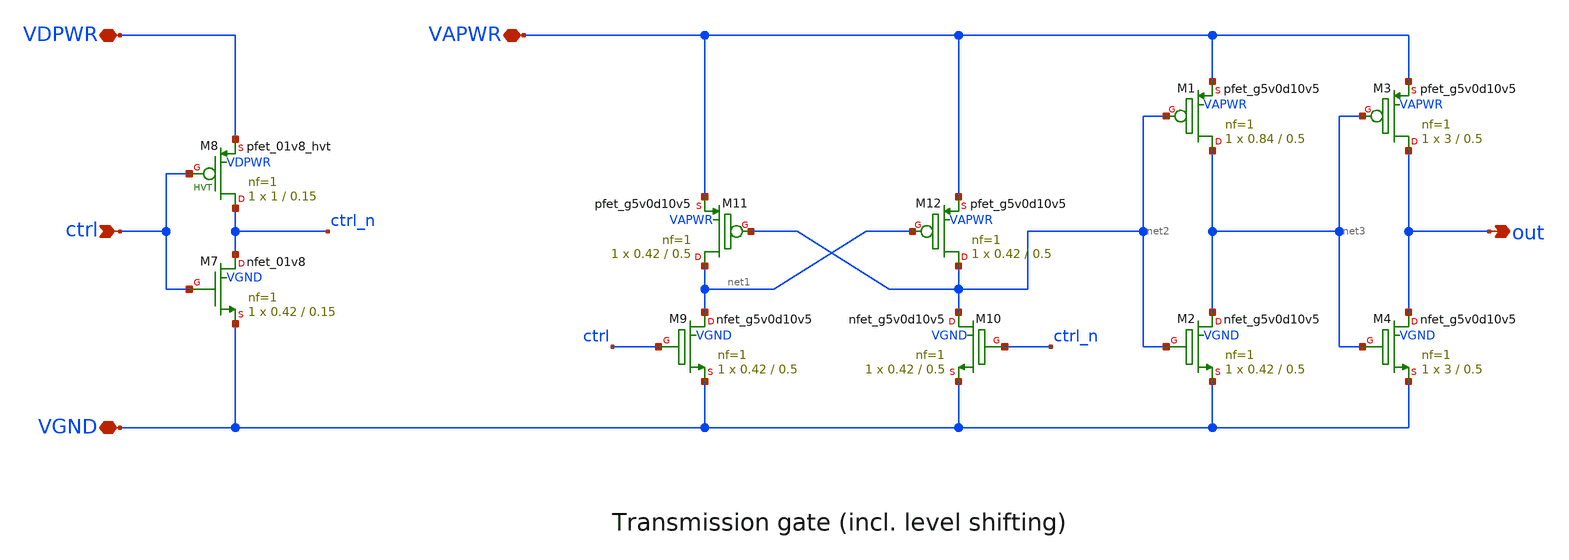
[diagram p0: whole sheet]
** sch_path: xschem/dac_drive.sch
**.subckt dac_drive ctrl VGND VDPWR VAPWR out
*.ipin ctrl
*.iopin VGND
*.iopin VDPWR
*.iopin VAPWR
*.opin out
XM1 net3 net2 VAPWR VAPWR sky130_fd_pr__pfet_g5v0d10v5 L=0.5 W=0.84 nf=1 ad='int((nf+1)/2) * W/nf * 0.29'
+ as='int((nf+2)/2) * W/nf * 0.29' pd='2*int((nf+1)/2) * (W/nf + 0.29)' ps='2*int((nf+2)/2) * (W/nf + 0.29)'
+ nrd='0.29 / W' nrs='0.29 / W' sa=0 sb=0 sd=0 mult=1 m=1
XM2 net3 net2 VGND VGND sky130_fd_pr__nfet_g5v0d10v5 L=0.5 W=0.42 nf=1 ad='int((nf+1)/2) * W/nf * 0.29'
+ as='int((nf+2)/2) * W/nf * 0.29' pd='2*int((nf+1)/2) * (W/nf + 0.29)' ps='2*int((nf+2)/2) * (W/nf + 0.29)'
+ nrd='0.29 / W' nrs='0.29 / W' sa=0 sb=0 sd=0 mult=1 m=1
XM7 ctrl_n ctrl VGND VGND sky130_fd_pr__nfet_01v8 L=0.15 W=0.42 nf=1 ad='int((nf+1)/2) * W/nf * 0.29'
+ as='int((nf+2)/2) * W/nf * 0.29' pd='2*int((nf+1)/2) * (W/nf + 0.29)' ps='2*int((nf+2)/2) * (W/nf + 0.29)'
+ nrd='0.29 / W' nrs='0.29 / W' sa=0 sb=0 sd=0 mult=1 m=1
XM8 ctrl_n ctrl VDPWR VDPWR sky130_fd_pr__pfet_01v8_hvt L=0.15 W=1 nf=1 ad='int((nf+1)/2) * W/nf * 0.29'
+ as='int((nf+2)/2) * W/nf * 0.29' pd='2*int((nf+1)/2) * (W/nf + 0.29)' ps='2*int((nf+2)/2) * (W/nf + 0.29)'
+ nrd='0.29 / W' nrs='0.29 / W' sa=0 sb=0 sd=0 mult=1 m=1
XM9 net1 ctrl VGND VGND sky130_fd_pr__nfet_g5v0d10v5 L=0.5 W=0.42 nf=1 ad='int((nf+1)/2) * W/nf * 0.29'
+ as='int((nf+2)/2) * W/nf * 0.29' pd='2*int((nf+1)/2) * (W/nf + 0.29)' ps='2*int((nf+2)/2) * (W/nf + 0.29)'
+ nrd='0.29 / W' nrs='0.29 / W' sa=0 sb=0 sd=0 mult=1 m=1
XM10 net2 ctrl_n VGND VGND sky130_fd_pr__nfet_g5v0d10v5 L=0.5 W=0.42 nf=1 ad='int((nf+1)/2) * W/nf * 0.29'
+ as='int((nf+2)/2) * W/nf * 0.29' pd='2*int((nf+1)/2) * (W/nf + 0.29)' ps='2*int((nf+2)/2) * (W/nf + 0.29)'
+ nrd='0.29 / W' nrs='0.29 / W' sa=0 sb=0 sd=0 mult=1 m=1
XM11 net1 net2 VAPWR VAPWR sky130_fd_pr__pfet_g5v0d10v5 L=0.5 W=0.42 nf=1 ad='int((nf+1)/2) * W/nf * 0.29'
+ as='int((nf+2)/2) * W/nf * 0.29' pd='2*int((nf+1)/2) * (W/nf + 0.29)' ps='2*int((nf+2)/2) * (W/nf + 0.29)'
+ nrd='0.29 / W' nrs='0.29 / W' sa=0 sb=0 sd=0 mult=1 m=1
XM12 net2 net1 VAPWR VAPWR sky130_fd_pr__pfet_g5v0d10v5 L=0.5 W=0.42 nf=1 ad='int((nf+1)/2) * W/nf * 0.29'
+ as='int((nf+2)/2) * W/nf * 0.29' pd='2*int((nf+1)/2) * (W/nf + 0.29)' ps='2*int((nf+2)/2) * (W/nf + 0.29)'
+ nrd='0.29 / W' nrs='0.29 / W' sa=0 sb=0 sd=0 mult=1 m=1
XM3 out net3 VAPWR VAPWR sky130_fd_pr__pfet_g5v0d10v5 L=0.5 W=3 nf=1 ad='int((nf+1)/2) * W/nf * 0.29'
+ as='int((nf+2)/2) * W/nf * 0.29' pd='2*int((nf+1)/2) * (W/nf + 0.29)' ps='2*int((nf+2)/2) * (W/nf + 0.29)'
+ nrd='0.29 / W' nrs='0.29 / W' sa=0 sb=0 sd=0 mult=1 m=1
XM4 out net3 VGND VGND sky130_fd_pr__nfet_g5v0d10v5 L=0.5 W=3 nf=1 ad='int((nf+1)/2) * W/nf * 0.29' as='int((nf+2)/2) * W/nf * 0.29'
+ pd='2*int((nf+1)/2) * (W/nf + 0.29)' ps='2*int((nf+2)/2) * (W/nf + 0.29)' nrd='0.29 / W' nrs='0.29 / W'
+ sa=0 sb=0 sd=0 mult=1 m=1
**.ends
.end
